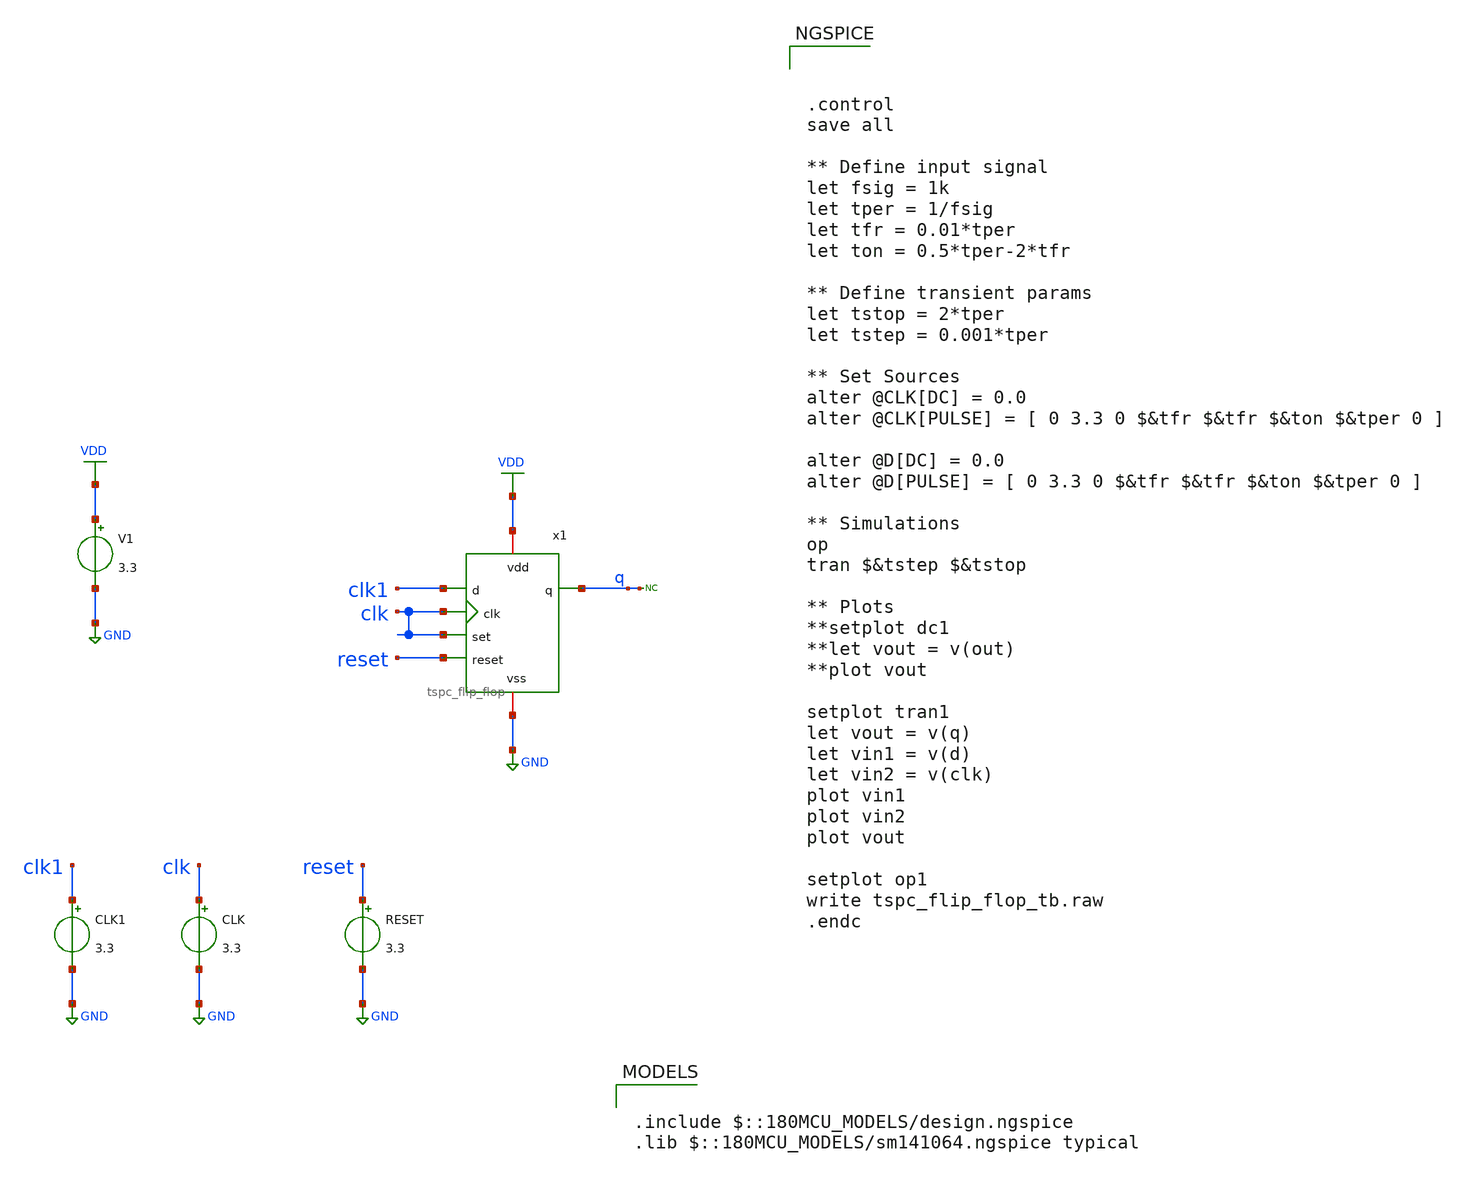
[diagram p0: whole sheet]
** sch_path: designs/libs/tspc_flip_flop/tspc_flip_flop_tb.sch
**.subckt tspc_flip_flop_tb
V1 VDD GND 3.3
CLK clk GND 3.3
RESET reset GND 3.3
* noconn q
CLK1 clk1 GND 3.3
x1 VDD GND clk1 clk clk reset q tspc_flip_flop
**** begin user architecture code

.include $::180MCU_MODELS/design.ngspice
.lib $::180MCU_MODELS/sm141064.ngspice typical




.control
save all

** Define input signal
let fsig = 1k
let tper = 1/fsig
let tfr = 0.01*tper
let ton = 0.5*tper-2*tfr

** Define transient params
let tstop = 2*tper
let tstep = 0.001*tper

** Set Sources
alter @CLK[DC] = 0.0
alter @CLK[PULSE] = [ 0 3.3 0 $&tfr $&tfr $&ton $&tper 0 ]

alter @D[DC] = 0.0
alter @D[PULSE] = [ 0 3.3 0 $&tfr $&tfr $&ton $&tper 0 ]

** Simulations
op
tran $&tstep $&tstop

** Plots
**setplot dc1
**let vout = v(out)
**plot vout

setplot tran1
let vout = v(q)
let vin1 = v(d)
let vin2 = v(clk)
plot vin1
plot vin2
plot vout

setplot op1
write tspc_flip_flop_tb.raw
.endc


**** end user architecture code
**.ends

* expanding   symbol:  tspc_flip_flop.sym # of pins=7
** sym_path: designs/libs/tspc_flip_flop/tspc_flip_flop.sym
** sch_path: designs/libs/tspc_flip_flop/tspc_flip_flop.sch
.subckt tspc_flip_flop vdd vss d clk set reset q
*.iopin vdd
*.iopin vss
*.ipin d
*.ipin clk
*.ipin set
*.ipin reset
*.opin q
XM1 b1 d vss vss nfet_03v3 L=0.28u W=1u nf=1 ad='int((nf+1)/2) * W/nf * 0.18u' as='int((nf+2)/2) * W/nf * 0.18u'
+ pd='2*int((nf+1)/2) * (W/nf + 0.18u)' ps='2*int((nf+2)/2) * (W/nf + 0.18u)' nrd='0.18u / W' nrs='0.18u / W'
+ sa=0 sb=0 sd=0 m=1
XM2 b1 clk net1 net1 pfet_03v3 L=0.28u W=4u nf=1 ad='int((nf+1)/2) * W/nf * 0.18u' as='int((nf+2)/2) * W/nf * 0.18u'
+ pd='2*int((nf+1)/2) * (W/nf + 0.18u)' ps='2*int((nf+2)/2) * (W/nf + 0.18u)' nrd='0.18u / W' nrs='0.18u / W'
+ sa=0 sb=0 sd=0 m=1
XM3 net1 d vdd vdd pfet_03v3 L=0.28u W=4u nf=1 ad='int((nf+1)/2) * W/nf * 0.18u' as='int((nf+2)/2) * W/nf * 0.18u'
+ pd='2*int((nf+1)/2) * (W/nf + 0.18u)' ps='2*int((nf+2)/2) * (W/nf + 0.18u)' nrd='0.18u / W' nrs='0.18u / W'
+ sa=0 sb=0 sd=0 m=1
XM4 b2 clk vdd vdd pfet_03v3 L=0.28u W=20u nf=1 ad='int((nf+1)/2) * W/nf * 0.18u' as='int((nf+2)/2) * W/nf * 0.18u'
+ pd='2*int((nf+1)/2) * (W/nf + 0.18u)' ps='2*int((nf+2)/2) * (W/nf + 0.18u)' nrd='0.18u / W' nrs='0.18u / W'
+ sa=0 sb=0 sd=0 m=1
XM5 b2 b1 net2 vss nfet_03v3 L=0.28u W=20u nf=1 ad='int((nf+1)/2) * W/nf * 0.18u' as='int((nf+2)/2) * W/nf * 0.18u'
+ pd='2*int((nf+1)/2) * (W/nf + 0.18u)' ps='2*int((nf+2)/2) * (W/nf + 0.18u)' nrd='0.18u / W' nrs='0.18u / W'
+ sa=0 sb=0 sd=0 m=1
XM6 net2 clk vss vss nfet_03v3 L=0.28u W=20u nf=1 ad='int((nf+1)/2) * W/nf * 0.18u' as='int((nf+2)/2) * W/nf * 0.18u'
+ pd='2*int((nf+1)/2) * (W/nf + 0.18u)' ps='2*int((nf+2)/2) * (W/nf + 0.18u)' nrd='0.18u / W' nrs='0.18u / W'
+ sa=0 sb=0 sd=0 m=1
XM7 net4 b2 vss vss nfet_03v3 L=0.28u W=80u nf=1 ad='int((nf+1)/2) * W/nf * 0.18u' as='int((nf+2)/2) * W/nf * 0.18u'
+ pd='2*int((nf+1)/2) * (W/nf + 0.18u)' ps='2*int((nf+2)/2) * (W/nf + 0.18u)' nrd='0.18u / W' nrs='0.18u / W'
+ sa=0 sb=0 sd=0 m=1
XM8 b3 clk net4 vss nfet_03v3 L=0.28u W=80u nf=1 ad='int((nf+1)/2) * W/nf * 0.18u' as='int((nf+2)/2) * W/nf * 0.18u'
+ pd='2*int((nf+1)/2) * (W/nf + 0.18u)' ps='2*int((nf+2)/2) * (W/nf + 0.18u)' nrd='0.18u / W' nrs='0.18u / W'
+ sa=0 sb=0 sd=0 m=1
XM9 b3 set net3 net3 pfet_03v3 L=0.28u W=80u nf=1 ad='int((nf+1)/2) * W/nf * 0.18u' as='int((nf+2)/2) * W/nf * 0.18u'
+ pd='2*int((nf+1)/2) * (W/nf + 0.18u)' ps='2*int((nf+2)/2) * (W/nf + 0.18u)' nrd='0.18u / W' nrs='0.18u / W'
+ sa=0 sb=0 sd=0 m=1
XM10 net3 b2 vdd vdd pfet_03v3 L=0.28u W=80u nf=1 ad='int((nf+1)/2) * W/nf * 0.18u' as='int((nf+2)/2) * W/nf * 0.18u'
+ pd='2*int((nf+1)/2) * (W/nf + 0.18u)' ps='2*int((nf+2)/2) * (W/nf + 0.18u)' nrd='0.18u / W' nrs='0.18u / W'
+ sa=0 sb=0 sd=0 m=1
XM11 b3 reset vdd vdd pfet_03v3 L=0.28u W=0.22u nf=1 ad='int((nf+1)/2) * W/nf * 0.18u' as='int((nf+2)/2) * W/nf * 0.18u'
+ pd='2*int((nf+1)/2) * (W/nf + 0.18u)' ps='2*int((nf+2)/2) * (W/nf + 0.18u)' nrd='0.18u / W' nrs='0.18u / W'
+ sa=0 sb=0 sd=0 m=1
XM12 b3 set vss vss nfet_03v3 L=0.28u W=0.22u nf=1 ad='int((nf+1)/2) * W/nf * 0.18u' as='int((nf+2)/2) * W/nf * 0.18u'
+ pd='2*int((nf+1)/2) * (W/nf + 0.18u)' ps='2*int((nf+2)/2) * (W/nf + 0.18u)' nrd='0.18u / W' nrs='0.18u / W'
+ sa=0 sb=0 sd=0 m=1
XM13 q b3 vdd vdd pfet_03v3 L=0.28u W=0.22u nf=1 ad='int((nf+1)/2) * W/nf * 0.18u' as='int((nf+2)/2) * W/nf * 0.18u'
+ pd='2*int((nf+1)/2) * (W/nf + 0.18u)' ps='2*int((nf+2)/2) * (W/nf + 0.18u)' nrd='0.18u / W' nrs='0.18u / W'
+ sa=0 sb=0 sd=0 m=1
XM14 q b3 vss vss nfet_03v3 L=0.28u W=0.22u nf=1 ad='int((nf+1)/2) * W/nf * 0.18u' as='int((nf+2)/2) * W/nf * 0.18u'
+ pd='2*int((nf+1)/2) * (W/nf + 0.18u)' ps='2*int((nf+2)/2) * (W/nf + 0.18u)' nrd='0.18u / W' nrs='0.18u / W'
+ sa=0 sb=0 sd=0 m=1
.ends

.GLOBAL GND
.GLOBAL VDD
.end
